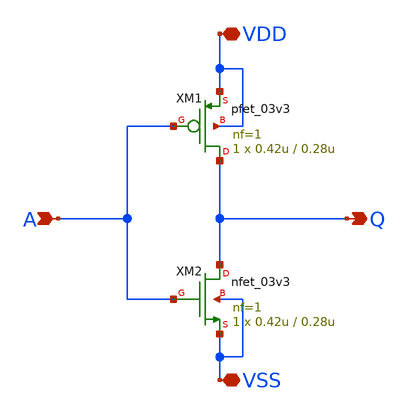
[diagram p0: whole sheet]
** sch_path: samples/inverter/GF180/inverter.sch
**.subckt inverter Q A VDD VSS
*.opin Q
*.ipin A
*.iopin VDD
*.iopin VSS
XM1 Q A VDD VDD pfet_03v3 L=0.28u W=0.42u nf=1 ad='int((nf+1)/2) * W/nf * 0.18u' as='int((nf+2)/2) * W/nf * 0.18u'
+ pd='2*int((nf+1)/2) * (W/nf + 0.18u)' ps='2*int((nf+2)/2) * (W/nf + 0.18u)' nrd='0.18u / W' nrs='0.18u / W'
+ sa=0 sb=0 sd=0 m=1
XM2 Q A VSS VSS nfet_03v3 L=0.28u W=0.42u nf=1 ad='int((nf+1)/2) * W/nf * 0.18u' as='int((nf+2)/2) * W/nf * 0.18u'
+ pd='2*int((nf+1)/2) * (W/nf + 0.18u)' ps='2*int((nf+2)/2) * (W/nf + 0.18u)' nrd='0.18u / W' nrs='0.18u / W'
+ sa=0 sb=0 sd=0 m=1
**.ends
.end
